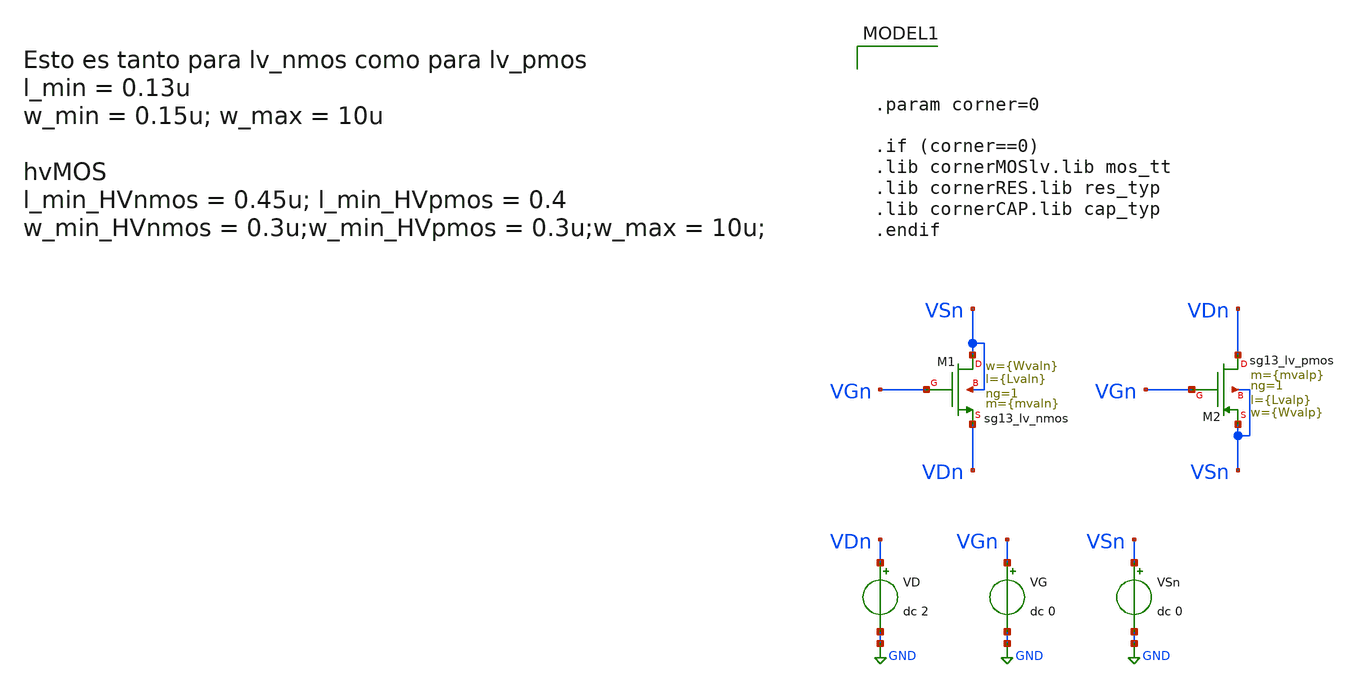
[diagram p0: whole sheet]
** sch_path: Esquematicos_Xschem/Memoria_NMOS_PMOS_COMP.sch
**.subckt Memoria_NMOS_PMOS_COMP
VG VGn GND dc 0
.save i(vg)
VD VDn GND dc 2
.save i(vd)
VSn VSn GND dc 0
.save i(vsn)
XM1 VSn VGn VDn VSn sg13_lv_nmos w={Wvaln} l={Lvaln} ng=1 m={mvaln} mm_ok=1
XM2 VDn VGn VSn VSn sg13_lv_pmos w={Wvalp} l={Lvalp} ng=1 m={mvalp} mm_ok=1
**** begin user architecture code




.option wnflag=1              ; Activa opción de simulación (warnings/flags específicos)
.savecurrents                 ; Guarda corrientes de nodos en la simulación

* ============================================================
* PARÁMETROS DE DISPOSITIVOS
* ============================================================
.param Lvaln = 0.2u           ; Longitud canal NMOS
.param Lvalp = 0.2u           ; Longitud canal PMOS
.param Wvaln = 0.6u            ; Ancho canal NMOS
.param Wvalp = 1.78u           ; Ancho canal PMOS
.param mvaln = 1              ; Multiplicidad NMOS
.param mvalp = 1              ; Multiplicidad PMOS


* ============================================================
* BLOQUE DE CONTROL DE SIMULACIÓN
* ============================================================
.control

  * Configuración general
  set filetype = ascii          ; Archivos de salida en formato ASCII
  set color0 = white            ; Fondo blanco en gráficas
  save all                      ; Guarda todas las variables de la simulación

  * Variables guardadas de NMOS y PMOS
  save @n.xm1.nsg13_lv_nmos[ids]    ; Corriente drenador NMOS
  *save @n.xm1.nsg13_lv_nmos[lp_cox]
  *save @n.xm1.nsg13_lv_nmos[cdg]
  *save @n.xm1.nsg13_lv_nmos[csg]
  *save @n.xm1.nsg13_lv_nmos[cgs]
  *save @n.xm1.nsg13_lv_nmos[lp_cgovd]
  save @n.xm2.nsg13_lv_pmos[ids]    ; Corriente drenador PMOS
  save @n.xm1.nsg13_lv_nmos[gm]     ; Transconductancia NMOS
  save @n.xm2.nsg13_lv_pmos[gm]     ; Transconductancia PMOS
  save @n.xm1.nsg13_lv_nmos[gds]    ; Conductancia salida NMOS
  save @n.xm2.nsg13_lv_pmos[gds]    ; Conductancia salida PMOS
  save @n.xm1.nsg13_lv_nmos[vth]    ; Voltaje umbral NMOS
  save @n.xm2.nsg13_lv_pmos[vth]    ; Voltaje umbral PMOS

* ============================================================
* BARRIDO DC
* ============================================================
  dc vd -0.9 0.9 0.1 vg -0.9 0.9 0.1

    * Definición de variables internas
    let IDSn  = @n.xm1.nsg13_lv_nmos[ids]
    let IDSp  = @n.xm2.nsg13_lv_pmos[ids]
    let gmn   = @n.xm1.nsg13_lv_nmos[gm]
    let gmp   = @n.xm2.nsg13_lv_pmos[gm]
    let gdsn  = @n.xm1.nsg13_lv_nmos[gds]
    let gdsp  = @n.xm2.nsg13_lv_pmos[gds]
    let VTHn  = @n.xm1.nsg13_lv_nmos[vth]
    let VTHp  = @n.xm2.nsg13_lv_pmos[vth]
    *let Coxn  = @n.xm1.nsg13_lv_nmos[lp_cox]
    *let Cdgn  = @n.xm1.nsg13_lv_nmos[cdg]
    *let Covdn = @n.xm1.nsg13_lv_nmos[lp_cgovd]
    *let Cgsn  = @n.xm1.nsg13_lv_nmos[csg]
    *let Csgn =  @n.xm1.nsg13_lv_nmos[cgs]
    let VDSn  = VDn - VSn
    let VGSn  = VGn - VSn

    * Inicialización de vectores parametros
    let n     = length(IDSn)
    let tol_i = 1e-10
    let IDSna = 0*v(VDSn)/v(VDSn)
    let IDSpa = 0*v(VDSn)/v(VDSn)
    let IDSpa2= 0*v(VDSn)/v(VDSn)

    * Acondicionamiento de corrientes NMOS
    let i = 0
    while i < n
      if IDSn[i] < tol_i
        let IDSna[i] = tol_i
      else
        let IDSna[i] = IDSn[i]
      end
      let i = i + 1
    end

    * Acondicionamiento de corrientes PMOS
    let i = 0
    while i < n
      if IDSp[i] < 1e-10
        let IDSpa2[i] = 1e-10
      else
        let IDSpa2[i] = IDSp[i]
      end
      let IDSpa[n-1-i] = IDSpa2[i]
      let i = i + 1
    end

* ============================================================
* GRÁFICAS
* ============================================================
  plot IDSn IDSp vs v(VDSn)                                         ; Corrientes absolutas vs VDS
  plot IDSna IDSpa vs v(VDSn)                                       ; Corrientes acondicionadas
  plot abs(IDSna-IDSpa)/abs(IDSna) vs v(VDSn) ylimit 0 1                    ; Error relativo
  plot deriv(IDSna)/deriv(VDSn) deriv(IDSpa)/deriv(VDSn) vs v(VDSn) ; Resistencia instantanea de
+ canal


* ============================================================
* EXPORTACIÓN DE RESULTADOS
* ============================================================
  *write Memoria_NMOS_DC_L0-5uW0-15u.csv VDSn VGSn IDSn IDSp VTHn VTHp IDSna IDSpa

* ============================================================
* GRÁFICAS ADICIONALES (comentadas)
* ============================================================
  *plot gmn deriv(idsn) deriv(gmn) vs vds
  *plot gdsn vs vgs
  *plot 1/gdsn vs vgs ylimit 0 1G xlimit 0 0.5
  *plot log(idsn) vs vgs ylimit -20 -4
  *plot Coxn Cdgn Covdn Cgsn Csgn vs v(VGSn)

.endc




.param corner=0

.if (corner==0)
.lib cornerMOSlv.lib mos_tt
.lib cornerRES.lib res_typ
.lib cornerCAP.lib cap_typ
.endif

**** end user architecture code
**.ends
.GLOBAL GND
.end
